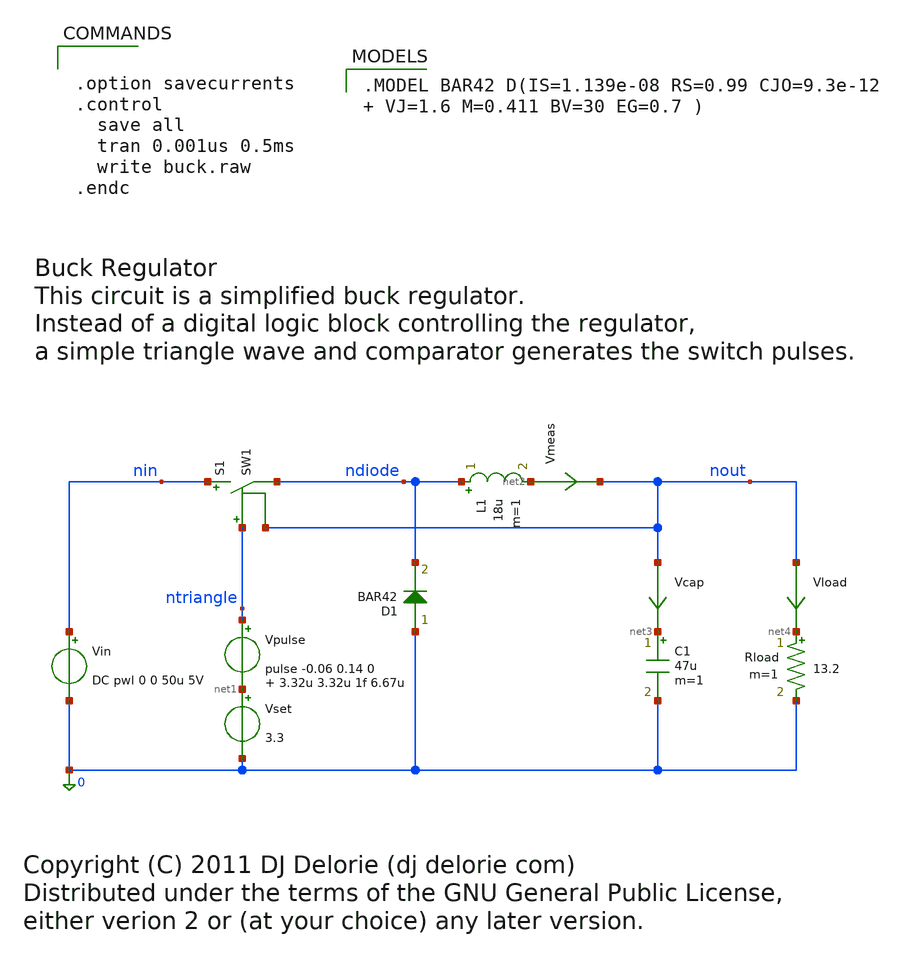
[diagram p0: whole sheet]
** sch_path: xschem_libraries_oa/ngspice/buck/schematic/buck.sch
* Copyright (C) 1998-2024 Stefan Frederik Schippers
* This program is free software; you can redistribute it and/or modify
* it under the terms of the GNU General Public License as published by
* the Free Software Foundation; either version 2 of the License, or
* (at your option) any later version.
* This program is distributed in the hope that it will be useful,
* but WITHOUT ANY WARRANTY; without even the implied warranty of
* MERCHANTABILITY or FITNESS FOR A PARTICULAR PURPOSE.  See the
* GNU General Public License for more details.
* You should have received a copy of the GNU General Public License
* along with this program; if not, write to the Free Software
* Copyright (C) 2011 DJ Delorie (dj delorie com)
* Distributed under the terms of the GNU General Public License,
* either verion 2 or (at your choice) any later version.
**.subckt buck
Vin nin 0 DC pwl 0 0 50u 5V
D1 0 ndiode BAR42 area=1
Vpulse ntriangle net1 pulse -0.06 0.14 0 3.32u 3.32u 1f 6.67u
Vset net1 0 3.3
Vmeas net2 nout 0
.save i(vmeas)
C1 net3 0 47u m=1
Vcap nout net3 0
.save i(vcap)
Vload nout net4 0
.save i(vload)
Rload net4 0 13.2 m=1
L1 ndiode net2 18u m=1
S1 nin ndiode ntriangle nout SW1
**** begin user architecture code

.MODEL BAR42 D(IS=1.139e-08 RS=0.99 CJO=9.3e-12  VJ=1.6 M=0.411 BV=30 EG=0.7 )




.option savecurrents
.control
  save all
  tran 0.001us 0.5ms
  write buck.raw
.endc


**** end user architecture code
**.ends
**** begin user architecture code
.MODEL SW1 SW   VT=0.0 VH=0.01  RON=0.001 ROFF=10G
**** end user architecture code
.end
